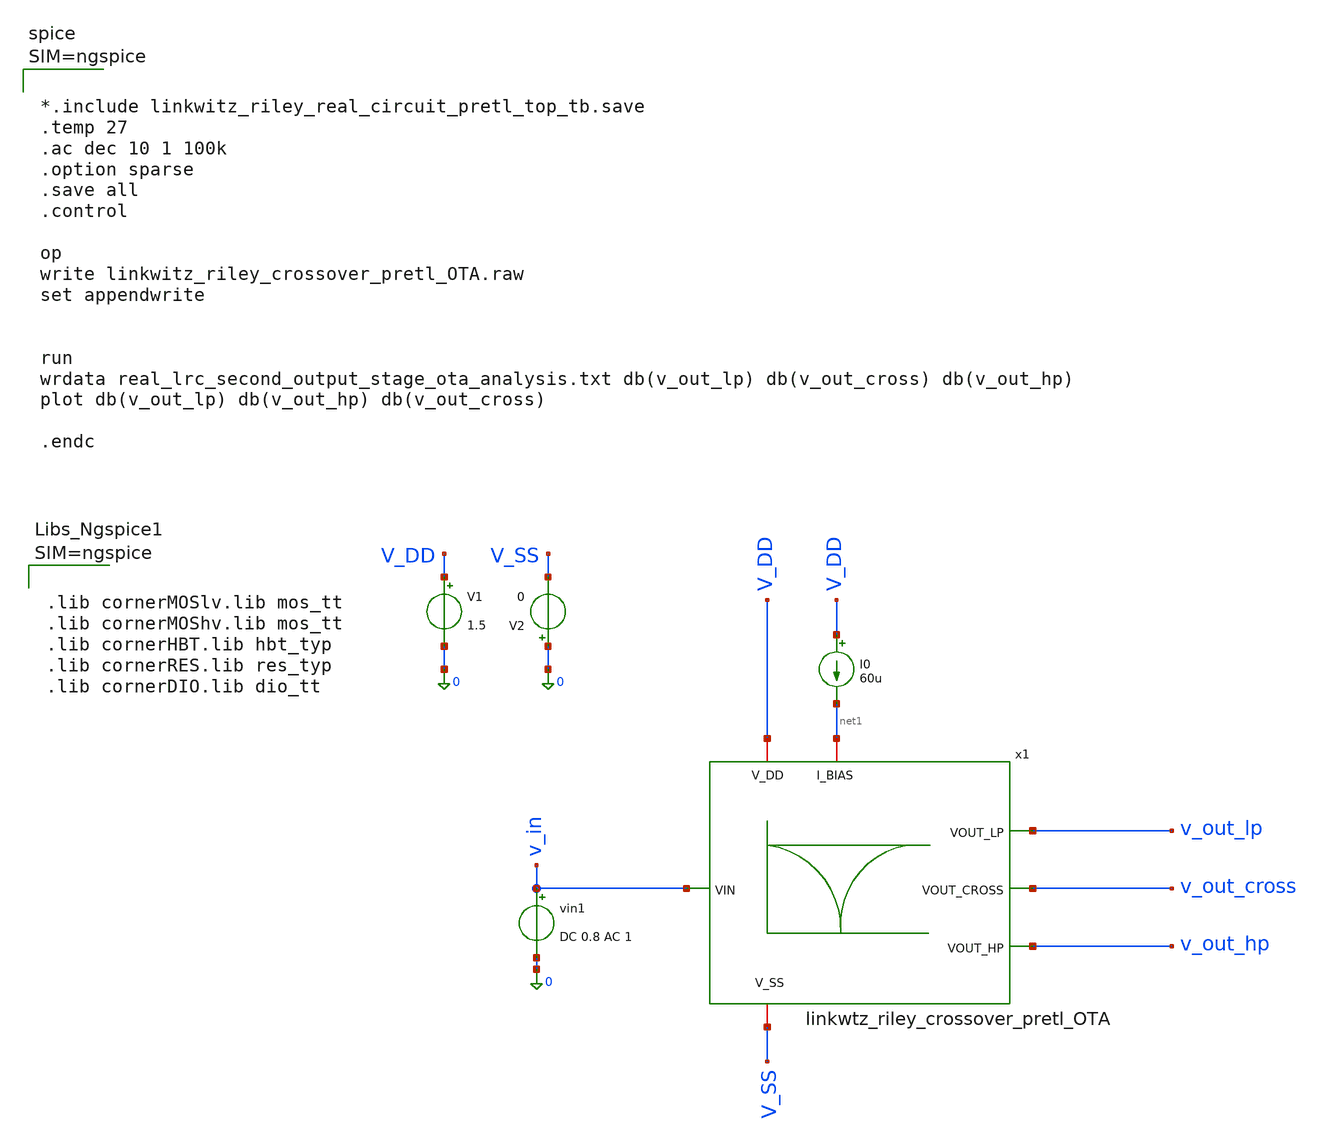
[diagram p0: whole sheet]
** sch_path: 004_Real_Circuits/003_version_second_output_stage/linkwitz_riley_real_circuit_pretl_top_tb.sch
**.subckt linkwitz_riley_real_circuit_pretl_top_tb
I0 V_DD net1 60u
V1 V_DD 0 1.5
vin1 v_in 0 DC 0.8 AC 1
V2 0 V_SS 0
x1 v_out_lp net1 V_DD v_out_cross V_SS v_in v_out_hp linkwtz_riley_crossover_pretl_OTA
**** begin user architecture code



.lib cornerMOSlv.lib mos_tt
.lib cornerMOShv.lib mos_tt
.lib cornerHBT.lib hbt_typ
.lib cornerRES.lib res_typ
.lib cornerDIO.lib dio_tt






*.include linkwitz_riley_real_circuit_pretl_top_tb.save
.temp 27
.ac dec 10 1 100k
.option sparse
.save all
.control

op
write linkwitz_riley_crossover_pretl_OTA.raw
set appendwrite


run
wrdata real_lrc_second_output_stage_ota_analysis.txt db(v_out_lp) db(v_out_cross) db(v_out_hp)
plot db(v_out_lp) db(v_out_hp) db(v_out_cross)

.endc



**** end user architecture code
**.ends
.end
